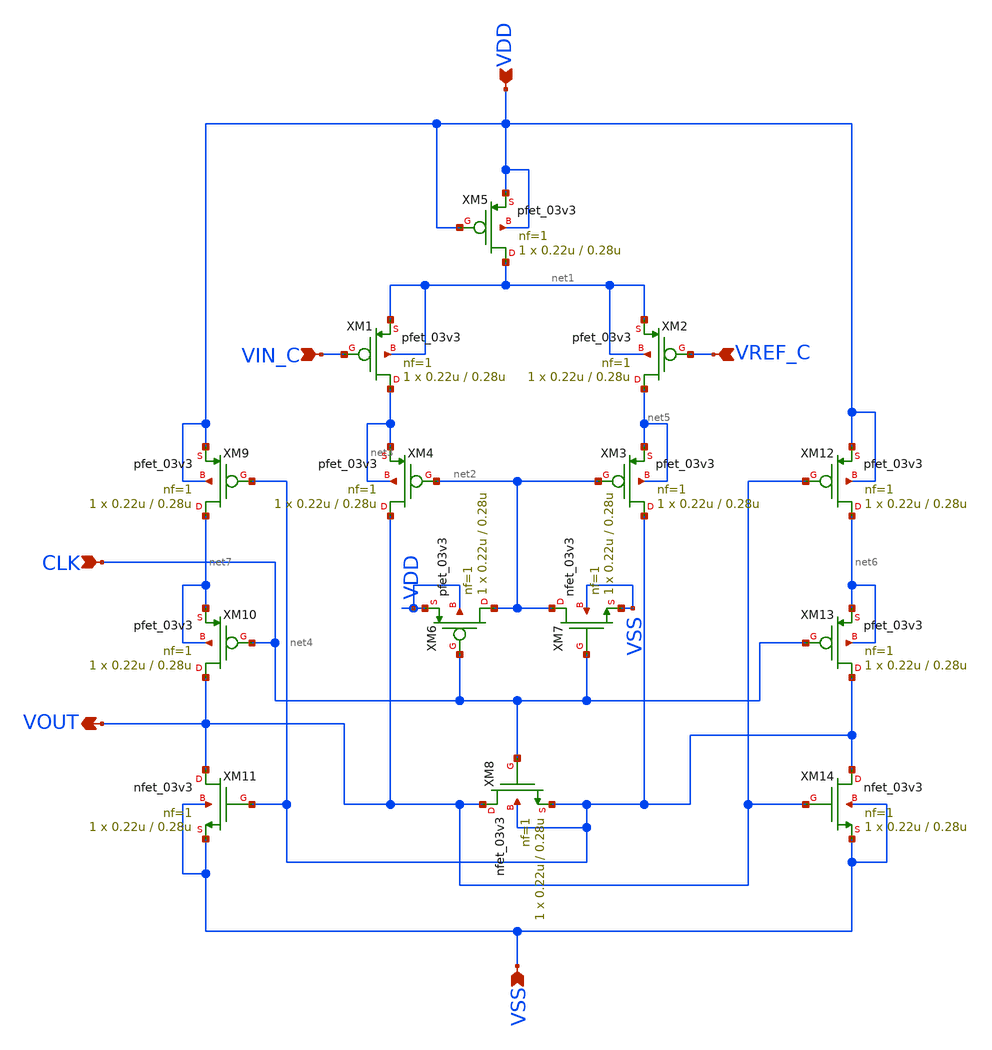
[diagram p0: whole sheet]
** sch_path: src/schematics/latched comparator/COMPARATOR_SD.sch
**.subckt COMPARATOR_SD VIN_C VREF_C CLK VOUT VDD VSS
*.ipin VIN_C
*.ipin VREF_C
*.ipin CLK
*.opin VOUT
*.ipin VDD
*.ipin VSS
XM5 net1 VDD VDD VDD pfet_03v3 L=0.28u W=0.22u nf=1 ad='int((nf+1)/2) * W/nf * 0.18u' as='int((nf+2)/2) * W/nf * 0.18u'
+ pd='2*int((nf+1)/2) * (W/nf + 0.18u)' ps='2*int((nf+2)/2) * (W/nf + 0.18u)' nrd='0.18u / W' nrs='0.18u / W'
+ sa=0 sb=0 sd=0 m=1
XM1 net3 VIN_C net1 net1 pfet_03v3 L=0.28u W=0.22u nf=1 ad='int((nf+1)/2) * W/nf * 0.18u' as='int((nf+2)/2) * W/nf * 0.18u'
+ pd='2*int((nf+1)/2) * (W/nf + 0.18u)' ps='2*int((nf+2)/2) * (W/nf + 0.18u)' nrd='0.18u / W' nrs='0.18u / W'
+ sa=0 sb=0 sd=0 m=1
XM2 net5 VREF_C net1 net1 pfet_03v3 L=0.28u W=0.22u nf=1 ad='int((nf+1)/2) * W/nf * 0.18u' as='int((nf+2)/2) * W/nf * 0.18u'
+ pd='2*int((nf+1)/2) * (W/nf + 0.18u)' ps='2*int((nf+2)/2) * (W/nf + 0.18u)' nrd='0.18u / W' nrs='0.18u / W'
+ sa=0 sb=0 sd=0 m=1
XM3 net4 net2 net5 net5 pfet_03v3 L=0.28u W=0.22u nf=1 ad='int((nf+1)/2) * W/nf * 0.18u' as='int((nf+2)/2) * W/nf * 0.18u'
+ pd='2*int((nf+1)/2) * (W/nf + 0.18u)' ps='2*int((nf+2)/2) * (W/nf + 0.18u)' nrd='0.18u / W' nrs='0.18u / W'
+ sa=0 sb=0 sd=0 m=1
XM4 VOUT net2 net3 net3 pfet_03v3 L=0.28u W=0.22u nf=1 ad='int((nf+1)/2) * W/nf * 0.18u' as='int((nf+2)/2) * W/nf * 0.18u'
+ pd='2*int((nf+1)/2) * (W/nf + 0.18u)' ps='2*int((nf+2)/2) * (W/nf + 0.18u)' nrd='0.18u / W' nrs='0.18u / W'
+ sa=0 sb=0 sd=0 m=1
XM6 net2 CLK VDD VDD pfet_03v3 L=0.28u W=0.22u nf=1 ad='int((nf+1)/2) * W/nf * 0.18u' as='int((nf+2)/2) * W/nf * 0.18u'
+ pd='2*int((nf+1)/2) * (W/nf + 0.18u)' ps='2*int((nf+2)/2) * (W/nf + 0.18u)' nrd='0.18u / W' nrs='0.18u / W'
+ sa=0 sb=0 sd=0 m=1
XM7 net2 CLK VSS VSS nfet_03v3 L=0.28u W=0.22u nf=1 ad='int((nf+1)/2) * W/nf * 0.18u' as='int((nf+2)/2) * W/nf * 0.18u'
+ pd='2*int((nf+1)/2) * (W/nf + 0.18u)' ps='2*int((nf+2)/2) * (W/nf + 0.18u)' nrd='0.18u / W' nrs='0.18u / W'
+ sa=0 sb=0 sd=0 m=1
XM8 VOUT CLK net4 net4 nfet_03v3 L=0.28u W=0.22u nf=1 ad='int((nf+1)/2) * W/nf * 0.18u' as='int((nf+2)/2) * W/nf * 0.18u'
+ pd='2*int((nf+1)/2) * (W/nf + 0.18u)' ps='2*int((nf+2)/2) * (W/nf + 0.18u)' nrd='0.18u / W' nrs='0.18u / W'
+ sa=0 sb=0 sd=0 m=1
XM9 net7 net4 VDD VDD pfet_03v3 L=0.28u W=0.22u nf=1 ad='int((nf+1)/2) * W/nf * 0.18u' as='int((nf+2)/2) * W/nf * 0.18u'
+ pd='2*int((nf+1)/2) * (W/nf + 0.18u)' ps='2*int((nf+2)/2) * (W/nf + 0.18u)' nrd='0.18u / W' nrs='0.18u / W'
+ sa=0 sb=0 sd=0 m=1
XM10 VOUT CLK net7 net7 pfet_03v3 L=0.28u W=0.22u nf=1 ad='int((nf+1)/2) * W/nf * 0.18u' as='int((nf+2)/2) * W/nf * 0.18u'
+ pd='2*int((nf+1)/2) * (W/nf + 0.18u)' ps='2*int((nf+2)/2) * (W/nf + 0.18u)' nrd='0.18u / W' nrs='0.18u / W'
+ sa=0 sb=0 sd=0 m=1
XM11 VOUT net4 VSS VSS nfet_03v3 L=0.28u W=0.22u nf=1 ad='int((nf+1)/2) * W/nf * 0.18u' as='int((nf+2)/2) * W/nf * 0.18u'
+ pd='2*int((nf+1)/2) * (W/nf + 0.18u)' ps='2*int((nf+2)/2) * (W/nf + 0.18u)' nrd='0.18u / W' nrs='0.18u / W'
+ sa=0 sb=0 sd=0 m=1
XM12 net6 VOUT VDD VDD pfet_03v3 L=0.28u W=0.22u nf=1 ad='int((nf+1)/2) * W/nf * 0.18u' as='int((nf+2)/2) * W/nf * 0.18u'
+ pd='2*int((nf+1)/2) * (W/nf + 0.18u)' ps='2*int((nf+2)/2) * (W/nf + 0.18u)' nrd='0.18u / W' nrs='0.18u / W'
+ sa=0 sb=0 sd=0 m=1
XM13 net4 CLK net6 net6 pfet_03v3 L=0.28u W=0.22u nf=1 ad='int((nf+1)/2) * W/nf * 0.18u' as='int((nf+2)/2) * W/nf * 0.18u'
+ pd='2*int((nf+1)/2) * (W/nf + 0.18u)' ps='2*int((nf+2)/2) * (W/nf + 0.18u)' nrd='0.18u / W' nrs='0.18u / W'
+ sa=0 sb=0 sd=0 m=1
XM14 net4 VOUT VSS VSS nfet_03v3 L=0.28u W=0.22u nf=1 ad='int((nf+1)/2) * W/nf * 0.18u' as='int((nf+2)/2) * W/nf * 0.18u'
+ pd='2*int((nf+1)/2) * (W/nf + 0.18u)' ps='2*int((nf+2)/2) * (W/nf + 0.18u)' nrd='0.18u / W' nrs='0.18u / W'
+ sa=0 sb=0 sd=0 m=1
**.ends
.end
